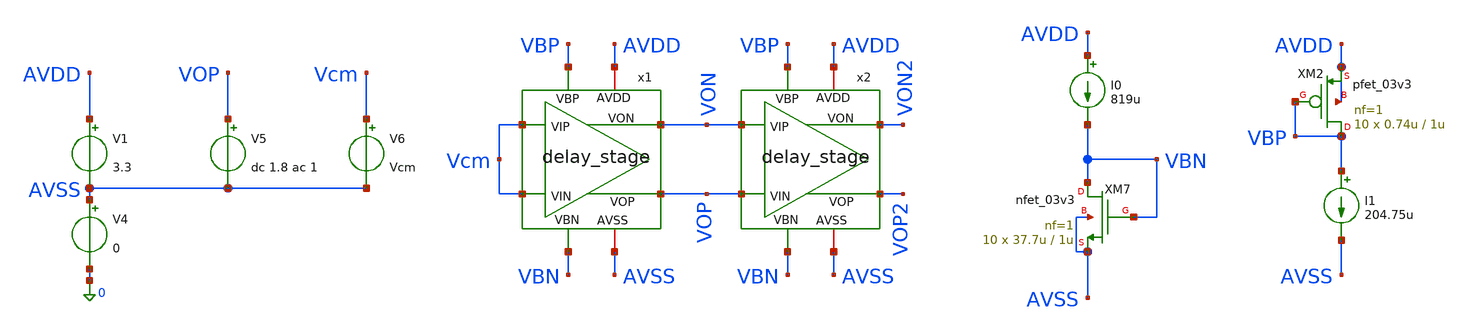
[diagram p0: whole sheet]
** sch_path: designs/libs/tb_analog/tb_delay_stage/tb_delay_stage_ac.sch
**.subckt tb_delay_stage_ac
x1 VOP AVDD Vcm Vcm VON AVSS VBP VBN delay_stage
V1 AVDD AVSS 3.3
V4 AVSS 0 0
V5 VOP AVSS dc 1.8 ac 1
V6 Vcm AVSS Vcm
x2 VOP2 AVDD VON VOP VON2 AVSS VBP VBN delay_stage
XM7 VBN VBN AVSS AVSS nfet_03v3 L=1u W=37.7u nf=1 ad='int((nf+1)/2) * W/nf * 0.18u' as='int((nf+2)/2) * W/nf * 0.18u'
+ pd='2*int((nf+1)/2) * (W/nf + 0.18u)' ps='2*int((nf+2)/2) * (W/nf + 0.18u)' nrd='0.18u / W' nrs='0.18u / W'
+ sa=0 sb=0 sd=0 m=10
I0 AVDD VBN 819u
XM2 VBP VBP AVDD AVDD pfet_03v3 L=1u W=0.74u nf=1 ad='int((nf+1)/2) * W/nf * 0.18u' as='int((nf+2)/2) * W/nf * 0.18u'
+ pd='2*int((nf+1)/2) * (W/nf + 0.18u)' ps='2*int((nf+2)/2) * (W/nf + 0.18u)' nrd='0.18u / W' nrs='0.18u / W'
+ sa=0 sb=0 sd=0 m=10
I1 VBP AVSS 204.75u
**** begin user architecture code


.param vbp=2.1 vbn=1.2 Vin=0 Vcm=1.8
* --- AC Impedance Extraction ---
.ac dec 10 1Meg 10G

.control
  run

  * Extract frequency vector
  let freq = frequency

  * Calculate angular frequency (omega)
  let omega = 2 * pi * freq

  * Calculate complex impedance Z = V / I
  * Note: v(VOP) is 1 (AC source), I is current through the AC source (e.g., v1)
  let Z = v(VOP) / -i(v5)

  * Extract imaginary part of admittance (Y = 1/Z)
  * Y_imag = omega * C
  let Y_imag = imag(1/Z)

  * Calculate effective capacitance
  let C_eff = Y_imag / omega

  * Plot capacitance over frequency to verify stability
  plot C_eff ylimit 0 300f

  * Print value at target operating frequency (e.g., 350 MHz)
  meas ac C_target FIND C_eff AT=350Meg

write tb_delay_stage_ac.raw
.endc



.include $::180MCU_MODELS/design.ngspice
.lib $::180MCU_MODELS/sm141064.ngspice typical

**** end user architecture code
**.ends

* expanding   symbol:  libs/core_analog/delay_stage/delay_stage.sym # of pins=8
** sym_path: designs/libs/core_analog/delay_stage/delay_stage.sym
** sch_path: designs/libs/core_analog/delay_stage/delay_stage.sch
.subckt delay_stage VOP AVDD VIP VIN VON AVSS VBP VBN
*.ipin VIP
*.ipin VIN
*.opin VOP
*.opin VON
*.iopin AVDD
*.iopin AVSS
*.ipin VBP
*.ipin VBN
XM5 VON VIP net1 AVSS nfet_03v3 L=0.5u W=2.08u nf=1 ad='int((nf+1)/2) * W/nf * 0.18u' as='int((nf+2)/2) * W/nf * 0.18u'
+ pd='2*int((nf+1)/2) * (W/nf + 0.18u)' ps='2*int((nf+2)/2) * (W/nf + 0.18u)' nrd='0.18u / W' nrs='0.18u / W'
+ sa=0 sb=0 sd=0 m=8
XM2 VON VON AVDD AVDD pfet_03v3 L=1.5u W=1.1u nf=1 ad='int((nf+1)/2) * W/nf * 0.18u' as='int((nf+2)/2) * W/nf * 0.18u'
+ pd='2*int((nf+1)/2) * (W/nf + 0.18u)' ps='2*int((nf+2)/2) * (W/nf + 0.18u)' nrd='0.18u / W' nrs='0.18u / W'
+ sa=0 sb=0 sd=0 m=8
XM6 VOP VIN net1 AVSS nfet_03v3 L=0.5u W=2.08u nf=1 ad='int((nf+1)/2) * W/nf * 0.18u' as='int((nf+2)/2) * W/nf * 0.18u'
+ pd='2*int((nf+1)/2) * (W/nf + 0.18u)' ps='2*int((nf+2)/2) * (W/nf + 0.18u)' nrd='0.18u / W' nrs='0.18u / W'
+ sa=0 sb=0 sd=0 m=8
XM1 VON VBP AVDD AVDD pfet_03v3 L=1.5u W=1.1u nf=1 ad='int((nf+1)/2) * W/nf * 0.18u' as='int((nf+2)/2) * W/nf * 0.18u'
+ pd='2*int((nf+1)/2) * (W/nf + 0.18u)' ps='2*int((nf+2)/2) * (W/nf + 0.18u)' nrd='0.18u / W' nrs='0.18u / W'
+ sa=0 sb=0 sd=0 m=8
XM3 VOP VBP AVDD AVDD pfet_03v3 L=1.5u W=1.1u nf=1 ad='int((nf+1)/2) * W/nf * 0.18u' as='int((nf+2)/2) * W/nf * 0.18u'
+ pd='2*int((nf+1)/2) * (W/nf + 0.18u)' ps='2*int((nf+2)/2) * (W/nf + 0.18u)' nrd='0.18u / W' nrs='0.18u / W'
+ sa=0 sb=0 sd=0 m=8
XM4 VOP VOP AVDD AVDD pfet_03v3 L=1.5u W=1.1u nf=1 ad='int((nf+1)/2) * W/nf * 0.18u' as='int((nf+2)/2) * W/nf * 0.18u'
+ pd='2*int((nf+1)/2) * (W/nf + 0.18u)' ps='2*int((nf+2)/2) * (W/nf + 0.18u)' nrd='0.18u / W' nrs='0.18u / W'
+ sa=0 sb=0 sd=0 m=8
XM8 net1 VBN AVSS AVSS nfet_03v3 L=0.5u W=11.25u nf=1 ad='int((nf+1)/2) * W/nf * 0.18u' as='int((nf+2)/2) * W/nf * 0.18u'
+ pd='2*int((nf+1)/2) * (W/nf + 0.18u)' ps='2*int((nf+2)/2) * (W/nf + 0.18u)' nrd='0.18u / W' nrs='0.18u / W'
+ sa=0 sb=0 sd=0 m=8
.ends

.end
